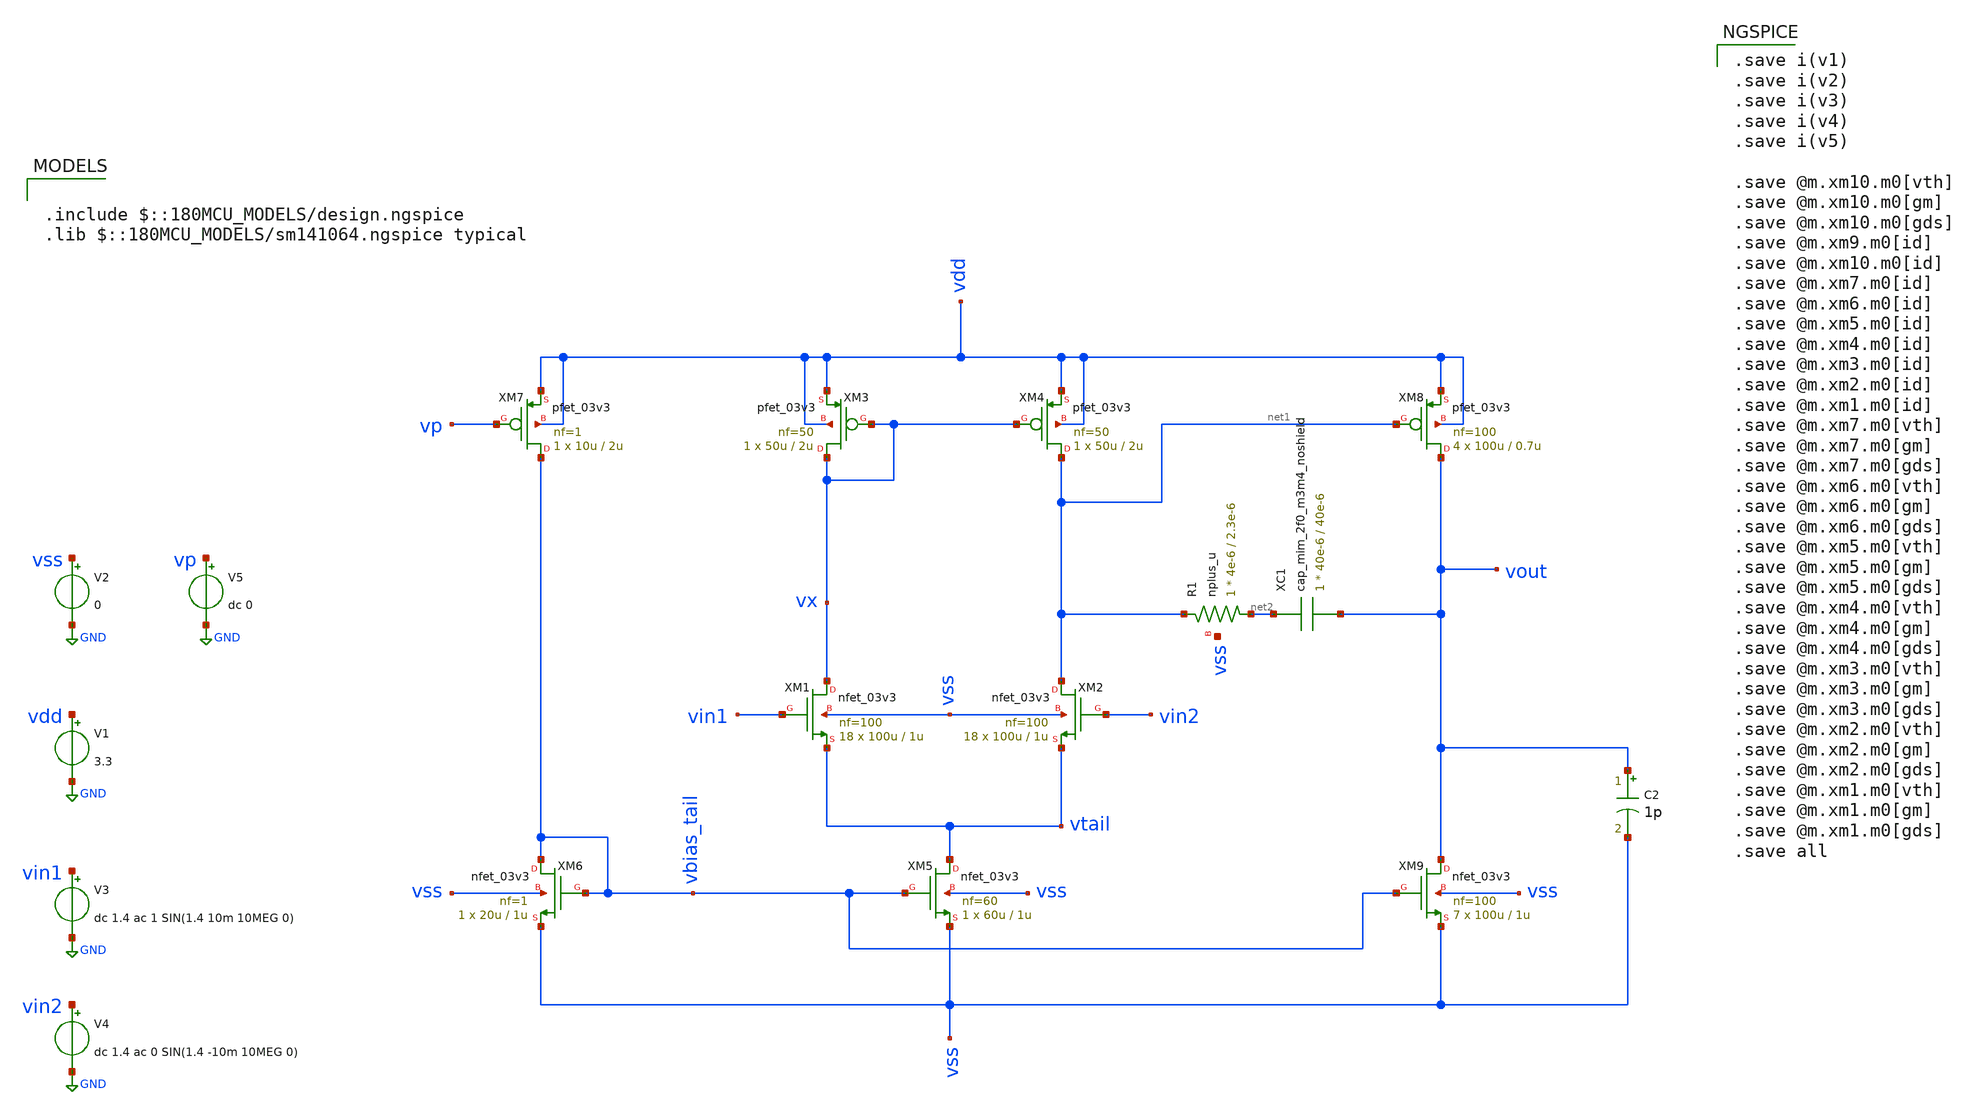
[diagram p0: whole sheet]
** sch_path: designs/comparator/preamp/tb_opamp.sch
**.subckt tb_opamp
V1 vdd GND 3.3
V3 vin1 GND dc 1.4 ac 1 SIN(1.4 10m 10MEG 0)
V4 vin2 GND dc 1.4 ac 0 SIN(1.4 -10m 10MEG 0)
V2 vss GND 0
V5 vp GND dc 0
XM1 vx vin1 vtail vss nfet_03v3 L=1u W=100u nf=100 ad='int((nf+1)/2) * W/nf * 0.18u' as='int((nf+2)/2) * W/nf * 0.18u'
+ pd='2*int((nf+1)/2) * (W/nf + 0.18u)' ps='2*int((nf+2)/2) * (W/nf + 0.18u)' nrd='0.18u / W' nrs='0.18u / W'
+ sa=0 sb=0 sd=0 m=18
XM2 net1 vin2 vtail vss nfet_03v3 L=1u W=100u nf=100 ad='int((nf+1)/2) * W/nf * 0.18u' as='int((nf+2)/2) * W/nf * 0.18u'
+ pd='2*int((nf+1)/2) * (W/nf + 0.18u)' ps='2*int((nf+2)/2) * (W/nf + 0.18u)' nrd='0.18u / W' nrs='0.18u / W'
+ sa=0 sb=0 sd=0 m=18
XM3 vx vx vdd vdd pfet_03v3 L=2u W=50u nf=50 ad='int((nf+1)/2) * W/nf * 0.18u' as='int((nf+2)/2) * W/nf * 0.18u'
+ pd='2*int((nf+1)/2) * (W/nf + 0.18u)' ps='2*int((nf+2)/2) * (W/nf + 0.18u)' nrd='0.18u / W' nrs='0.18u / W'
+ sa=0 sb=0 sd=0 m=1
XM4 net1 vx vdd vdd pfet_03v3 L=2u W=50u nf=50 ad='int((nf+1)/2) * W/nf * 0.18u' as='int((nf+2)/2) * W/nf * 0.18u'
+ pd='2*int((nf+1)/2) * (W/nf + 0.18u)' ps='2*int((nf+2)/2) * (W/nf + 0.18u)' nrd='0.18u / W' nrs='0.18u / W'
+ sa=0 sb=0 sd=0 m=1
XM5 vtail vbias_tail vss vss nfet_03v3 L=1u W=60u nf=60 ad='int((nf+1)/2) * W/nf * 0.18u' as='int((nf+2)/2) * W/nf * 0.18u'
+ pd='2*int((nf+1)/2) * (W/nf + 0.18u)' ps='2*int((nf+2)/2) * (W/nf + 0.18u)' nrd='0.18u / W' nrs='0.18u / W'
+ sa=0 sb=0 sd=0 m=1
XM6 vbias_tail vbias_tail vss vss nfet_03v3 L=1u W=20u nf=1 ad='int((nf+1)/2) * W/nf * 0.18u' as='int((nf+2)/2) * W/nf * 0.18u'
+ pd='2*int((nf+1)/2) * (W/nf + 0.18u)' ps='2*int((nf+2)/2) * (W/nf + 0.18u)' nrd='0.18u / W' nrs='0.18u / W'
+ sa=0 sb=0 sd=0 m=1
XM7 vbias_tail vp vdd vdd pfet_03v3 L=2u W=10u nf=1 ad='int((nf+1)/2) * W/nf * 0.18u' as='int((nf+2)/2) * W/nf * 0.18u'
+ pd='2*int((nf+1)/2) * (W/nf + 0.18u)' ps='2*int((nf+2)/2) * (W/nf + 0.18u)' nrd='0.18u / W' nrs='0.18u / W'
+ sa=0 sb=0 sd=0 m=1
XM8 vout net1 vdd vdd pfet_03v3 L=0.7u W=100u nf=100 ad='int((nf+1)/2) * W/nf * 0.18u' as='int((nf+2)/2) * W/nf * 0.18u'
+ pd='2*int((nf+1)/2) * (W/nf + 0.18u)' ps='2*int((nf+2)/2) * (W/nf + 0.18u)' nrd='0.18u / W' nrs='0.18u / W'
+ sa=0 sb=0 sd=0 m=4
XM9 vout vbias_tail vss vss nfet_03v3 L=1u W=100u nf=100 ad='int((nf+1)/2) * W/nf * 0.18u' as='int((nf+2)/2) * W/nf * 0.18u'
+ pd='2*int((nf+1)/2) * (W/nf + 0.18u)' ps='2*int((nf+2)/2) * (W/nf + 0.18u)' nrd='0.18u / W' nrs='0.18u / W'
+ sa=0 sb=0 sd=0 m=7
XR1 net2 net1 vss nplus_u r_width=4e-6 r_length=2.3e-6 m=1
C2 vout vss 1p m=1
XC1 net2 vout cap_mim_2f0_m3m4_noshield c_width=40e-6 c_length=40e-6 m=1
**** begin user architecture code

.include $::180MCU_MODELS/design.ngspice
.lib $::180MCU_MODELS/sm141064.ngspice typical


.save i(v1)
.save i(v2)
.save i(v3)
.save i(v4)
.save i(v5)

.save @m.xm10.m0[vth]
.save @m.xm10.m0[gm]
.save @m.xm10.m0[gds]
.save @m.xm9.m0[id]
.save @m.xm10.m0[id]
.save @m.xm7.m0[id]
.save @m.xm6.m0[id]
.save @m.xm5.m0[id]
.save @m.xm4.m0[id]
.save @m.xm3.m0[id]
.save @m.xm2.m0[id]
.save @m.xm1.m0[id]
.save @m.xm7.m0[vth]
.save @m.xm7.m0[gm]
.save @m.xm7.m0[gds]
.save @m.xm6.m0[vth]
.save @m.xm6.m0[gm]
.save @m.xm6.m0[gds]
.save @m.xm5.m0[vth]
.save @m.xm5.m0[gm]
.save @m.xm5.m0[gds]
.save @m.xm4.m0[vth]
.save @m.xm4.m0[gm]
.save @m.xm4.m0[gds]
.save @m.xm3.m0[vth]
.save @m.xm3.m0[gm]
.save @m.xm3.m0[gds]
.save @m.xm2.m0[vth]
.save @m.xm2.m0[gm]
.save @m.xm2.m0[gds]
.save @m.xm1.m0[vth]
.save @m.xm1.m0[gm]
.save @m.xm1.m0[gds]
.save all


.control
run
let a = 0
let b = 0
let step = 0.1
let final = 2
let test = a
let test1 = a
let cnt = 0
let ind = ((final-a)/step)
let n = vector(ind)
let power = vector(ind)

set color0 = white
set color1 = black
set hcopydevtype = svg
setcs svg_stropts = ( black Arial Arial )

set gain = ' '
set phasedeg = ' '
set tranout = ' '
set nolegend

while test le final
  alter @v5[dc] = test
  print @v5[dc]
  let test = test + step
  ac dec 10 1 300MEG
  let phase = {57.29*vp(vout)}-180
  set gain = ( $gain db({$curplot}.vout) )
  set phasedeg = ( $phasedeg ({$curplot}.phase) )
end

plot $gain xlabel Frequency(Hz) ylabel Gain(db) title Gain(dB)
plot $phasedeg xlabel Frequency(Hz) ylabel Phase(deg) title Phase(deg)

hardcopy Gain.svg $gain xlabel Frequency(Hz) ylabel Gain(db) title 'OTA_2stage Gain(ss)'
hardcopy Phase.svg $phasedeg xlabel Frequency(Hz) ylabel Phase(deg) title 'OTA_2stage Phase(ss)'

let test = a

while test le final
  alter @v5[dc] = test
  print @v5[dc]
  let test = test + step
  tran 1ns 500ns 0
  set tranout = ( $tranout ({$curplot}.vout) )
end

plot $tranout xlabel Time(ns) ylabel Output(V) title Output_Signal
hardcopy Transient.svg $tranout xlabel Time(ns) ylabel Output title 'OTA_2stage Transient Plot(ss)'

while test1 le final
  alter @v5[dc] = test1
  print @v5[dc]
  save all
  let ic = @m.xm5.m0[id] + @m.xm6.m0[id] + @m.xm9.m0[id]
  let power[cnt] = 3.3*ic
  let test1 = test1 + step
  noise v(vout) v3 dec 100 20K 2MEG 1
  let n[cnt] = inoise_total
  let cnt = cnt + 1
end

plot n vs power xlabel Power(mW) ylabel Integrated_Noise(uV) title Integrated_Noise

hardcopy Noise.svg n vs power xlabel Power(mW) ylabel Integrated_Noise(uV) title 'OTA_2stage Integrated_Noise(ss)'

.endc


**** end user architecture code
**.ends
.GLOBAL GND
.end
